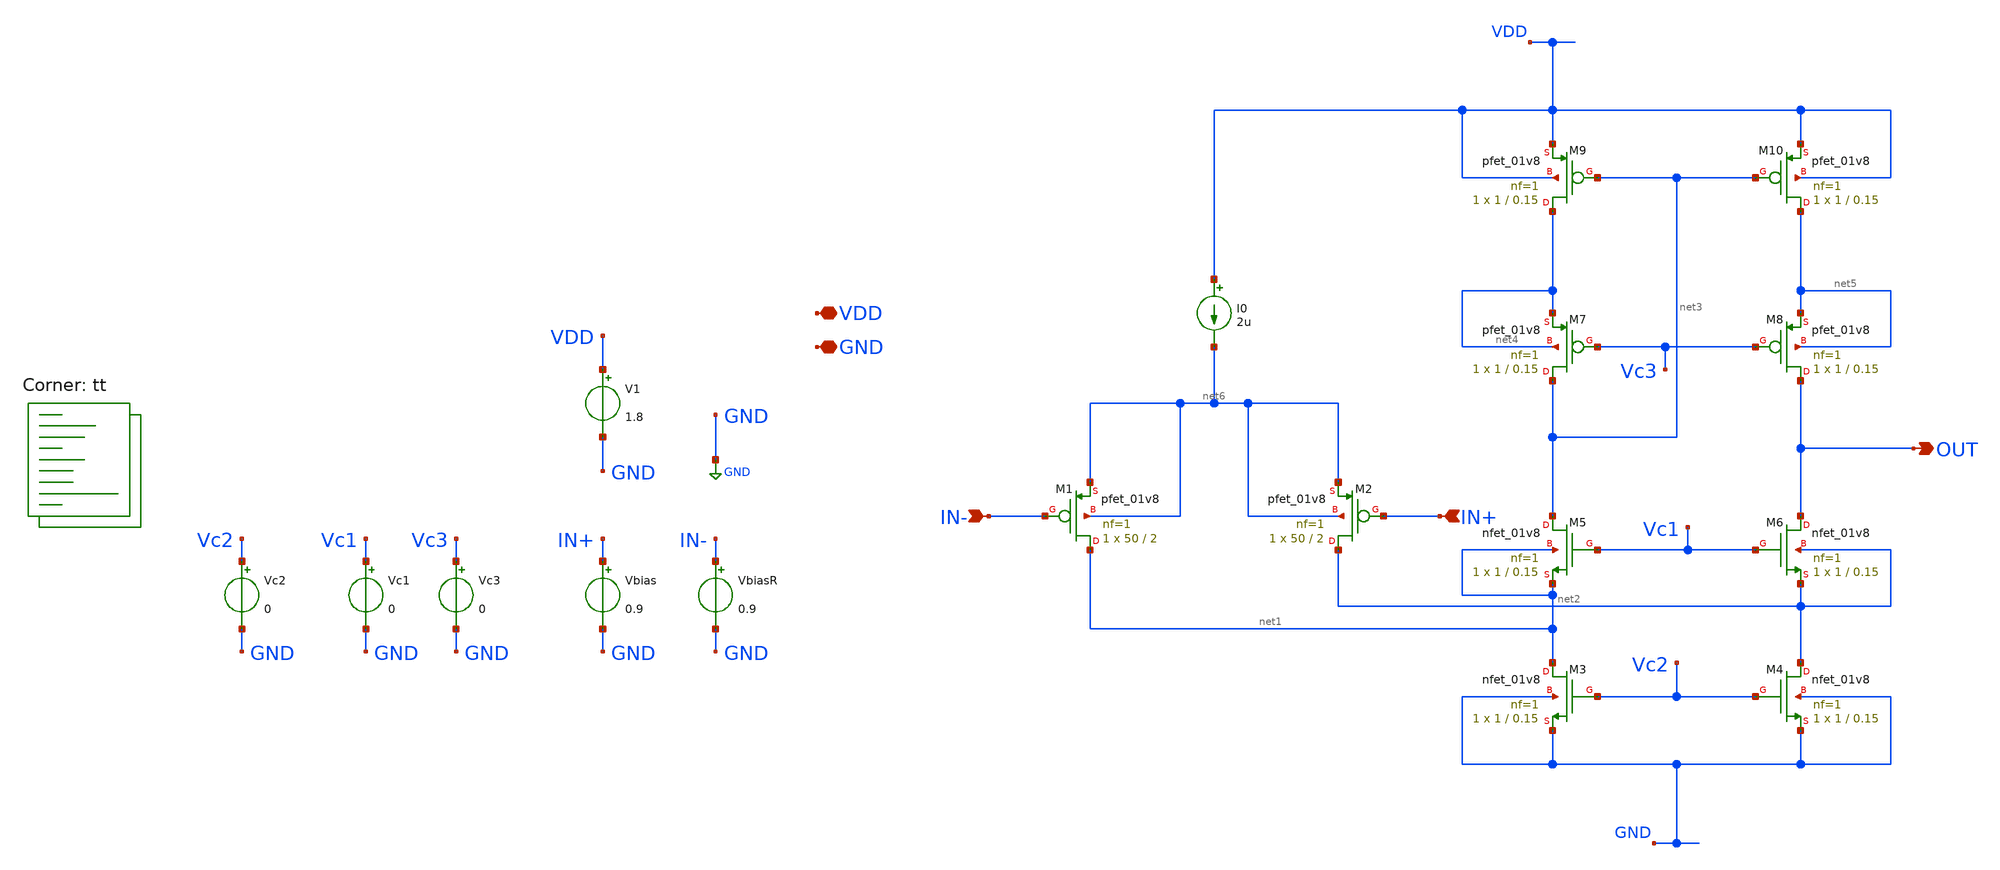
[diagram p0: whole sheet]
** sch_path: xschem/OTA_FoldedCascode.sch
**.subckt OTA_FoldedCascode VDD GND IN+ IN- OUT
*.iopin VDD
*.iopin GND
*.ipin IN+
*.ipin IN-
*.opin OUT
V1 VDD GND 1.8
Vbias IN+ GND 0.9
VbiasR IN- GND 0.9
I0 VDD net6 2u
XM1 net1 IN- net6 net6 sky130_fd_pr__pfet_01v8 L=2 W=50 nf=1 ad='int((nf+1)/2) * W/nf * 0.29' as='int((nf+2)/2) * W/nf * 0.29'
+ pd='2*int((nf+1)/2) * (W/nf + 0.29)' ps='2*int((nf+2)/2) * (W/nf + 0.29)' nrd='0.29 / W' nrs='0.29 / W'
+ sa=0 sb=0 sd=0 mult=1 m=1
XM2 net2 IN+ net6 net6 sky130_fd_pr__pfet_01v8 L=2 W=50 nf=1 ad='int((nf+1)/2) * W/nf * 0.29' as='int((nf+2)/2) * W/nf * 0.29'
+ pd='2*int((nf+1)/2) * (W/nf + 0.29)' ps='2*int((nf+2)/2) * (W/nf + 0.29)' nrd='0.29 / W' nrs='0.29 / W'
+ sa=0 sb=0 sd=0 mult=1 m=1
XM3 net1 Vc2 GND GND sky130_fd_pr__nfet_01v8 L=0.15 W=1 nf=1 ad='int((nf+1)/2) * W/nf * 0.29' as='int((nf+2)/2) * W/nf * 0.29'
+ pd='2*int((nf+1)/2) * (W/nf + 0.29)' ps='2*int((nf+2)/2) * (W/nf + 0.29)' nrd='0.29 / W' nrs='0.29 / W'
+ sa=0 sb=0 sd=0 mult=1 m=1
XM4 net2 Vc2 GND GND sky130_fd_pr__nfet_01v8 L=0.15 W=1 nf=1 ad='int((nf+1)/2) * W/nf * 0.29' as='int((nf+2)/2) * W/nf * 0.29'
+ pd='2*int((nf+1)/2) * (W/nf + 0.29)' ps='2*int((nf+2)/2) * (W/nf + 0.29)' nrd='0.29 / W' nrs='0.29 / W'
+ sa=0 sb=0 sd=0 mult=1 m=1
XM5 net3 Vc1 net1 net1 sky130_fd_pr__nfet_01v8 L=0.15 W=1 nf=1 ad='int((nf+1)/2) * W/nf * 0.29' as='int((nf+2)/2) * W/nf * 0.29'
+ pd='2*int((nf+1)/2) * (W/nf + 0.29)' ps='2*int((nf+2)/2) * (W/nf + 0.29)' nrd='0.29 / W' nrs='0.29 / W'
+ sa=0 sb=0 sd=0 mult=1 m=1
XM6 OUT Vc1 net2 net2 sky130_fd_pr__nfet_01v8 L=0.15 W=1 nf=1 ad='int((nf+1)/2) * W/nf * 0.29' as='int((nf+2)/2) * W/nf * 0.29'
+ pd='2*int((nf+1)/2) * (W/nf + 0.29)' ps='2*int((nf+2)/2) * (W/nf + 0.29)' nrd='0.29 / W' nrs='0.29 / W'
+ sa=0 sb=0 sd=0 mult=1 m=1
XM7 net3 Vc3 net4 net4 sky130_fd_pr__pfet_01v8 L=0.15 W=1 nf=1 ad='int((nf+1)/2) * W/nf * 0.29' as='int((nf+2)/2) * W/nf * 0.29'
+ pd='2*int((nf+1)/2) * (W/nf + 0.29)' ps='2*int((nf+2)/2) * (W/nf + 0.29)' nrd='0.29 / W' nrs='0.29 / W'
+ sa=0 sb=0 sd=0 mult=1 m=1
XM8 OUT Vc3 net5 net5 sky130_fd_pr__pfet_01v8 L=0.15 W=1 nf=1 ad='int((nf+1)/2) * W/nf * 0.29' as='int((nf+2)/2) * W/nf * 0.29'
+ pd='2*int((nf+1)/2) * (W/nf + 0.29)' ps='2*int((nf+2)/2) * (W/nf + 0.29)' nrd='0.29 / W' nrs='0.29 / W'
+ sa=0 sb=0 sd=0 mult=1 m=1
XM9 net4 net3 VDD VDD sky130_fd_pr__pfet_01v8 L=0.15 W=1 nf=1 ad='int((nf+1)/2) * W/nf * 0.29' as='int((nf+2)/2) * W/nf * 0.29'
+ pd='2*int((nf+1)/2) * (W/nf + 0.29)' ps='2*int((nf+2)/2) * (W/nf + 0.29)' nrd='0.29 / W' nrs='0.29 / W'
+ sa=0 sb=0 sd=0 mult=1 m=1
XM10 net5 net3 VDD VDD sky130_fd_pr__pfet_01v8 L=0.15 W=1 nf=1 ad='int((nf+1)/2) * W/nf * 0.29' as='int((nf+2)/2) * W/nf * 0.29'
+ pd='2*int((nf+1)/2) * (W/nf + 0.29)' ps='2*int((nf+2)/2) * (W/nf + 0.29)' nrd='0.29 / W' nrs='0.29 / W'
+ sa=0 sb=0 sd=0 mult=1 m=1
Vc1 Vc1 GND 0
Vc2 Vc2 GND 0
Vc3 Vc3 GND 0
**** begin user architecture code



* ngspice commands

.options savecurrents

.control
save all
save @m.xm1.msky130_fd_pr__pfet_01v8[gm]
save @m.xm2.msky130_fd_pr__pfet_01v8[gm]
save @m.xm3.msky130_fd_pr__nfet_01v8[gm]
save @m.xm4.msky130_fd_pr__nfet_01v8[gm]
save @m.xm5.msky130_fd_pr__nfet_01v8[gm]
save @m.xm6.msky130_fd_pr__nfet_01v8[gm]
save @m.xm7.msky130_fd_pr__pfet_01v8[gm]
save @m.xm8.msky130_fd_pr__pfet_01v8[gm]
save @m.xm9.msky130_fd_pr__pfet_01v8[gm]
save @m.xm10.msky130_fd_pr__pfet_01v8[gm]

   op
   remzerovec

   *dc Vbias 0 1.8 0.001

   *plot v(out),v(in+)
   *plot deriv(v(out))

   write OTA_FoldedCascode.raw
.endc




.lib $::SKYWATER_MODELS/sky130.lib.spice tt
**** end user architecture code
**.ends
.GLOBAL GND
.end
